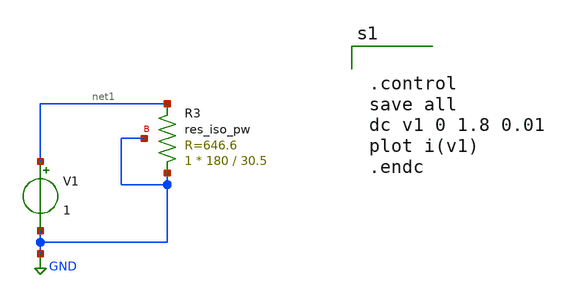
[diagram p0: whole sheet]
** sch_path: modules/testing_res/test/res_iso_corners.sch
**.subckt res_iso_corners
XR3 GND net1 GND sky130_fd_pr__res_iso_pw W=180 L=30.5 m=1
V1 net1 GND 1
**** begin user architecture code


.control
save all
dc v1 0 1.8 0.01
plot i(v1)
.endc



.lib $env(PDK_ROOT)/$env(PDK)/libs.tech/ngspice/sky130.lib.spice.tt.red tt
*.lib $env(PDK_ROOT)/$env(PDK)/libs.tech/combined/sky130.lib.spice tt

**** end user architecture code
**.ends
.GLOBAL GND
.end
